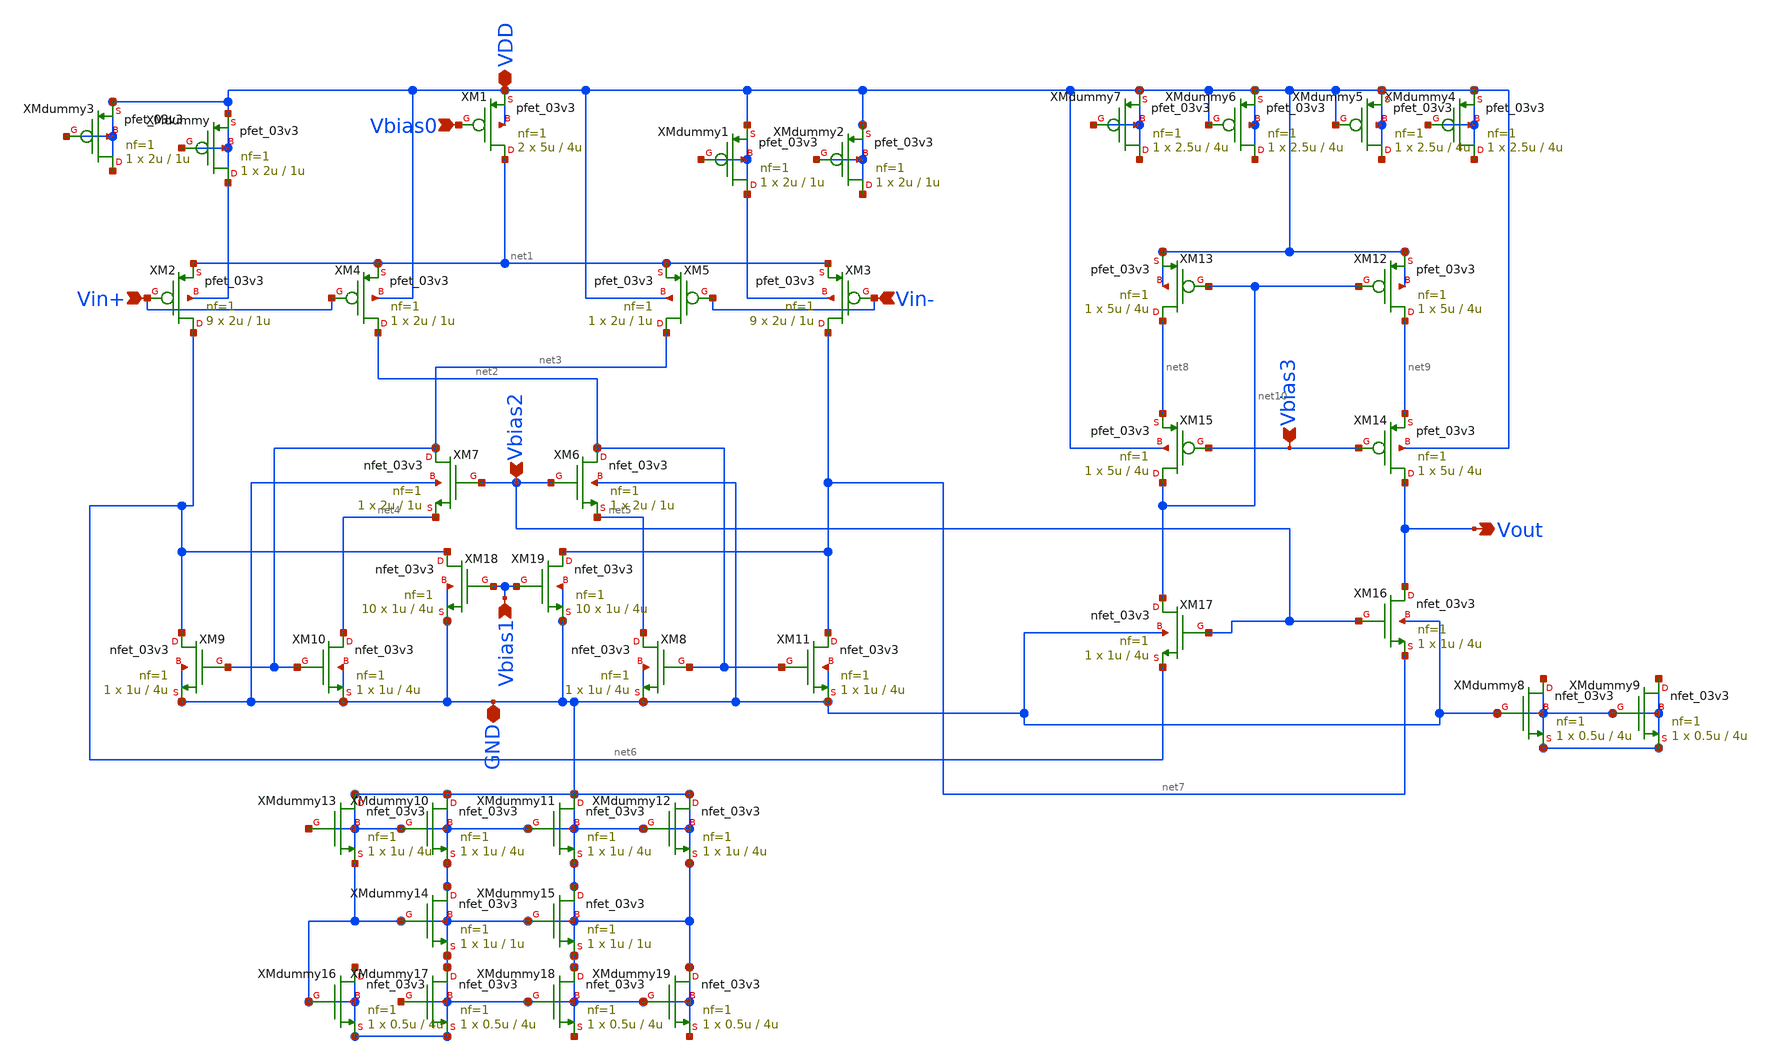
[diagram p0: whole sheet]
** sch_path: analog/B04_OTA.sch
**.subckt B04_OTA VDD Vbias0 Vin+ Vin- Vout Vbias3 Vbias2 GND Vbias1
*.iopin VDD
*.ipin Vbias0
*.ipin Vin+
*.ipin Vin-
*.opin Vout
*.ipin Vbias3
*.ipin Vbias2
*.iopin GND
*.ipin Vbias1
XM1 net1 Vbias0 VDD VDD pfet_03v3 L=4u W=5u nf=1 ad='int((nf+1)/2) * W/nf * 0.18u' as='int((nf+2)/2) * W/nf * 0.18u'
+ pd='2*int((nf+1)/2) * (W/nf + 0.18u)' ps='2*int((nf+2)/2) * (W/nf + 0.18u)' nrd='0.18u / W' nrs='0.18u / W'
+ sa=0 sb=0 sd=0 m=2
XM2 net6 Vin+ net1 VDD pfet_03v3 L=1u W=2u nf=1 ad='int((nf+1)/2) * W/nf * 0.18u' as='int((nf+2)/2) * W/nf * 0.18u'
+ pd='2*int((nf+1)/2) * (W/nf + 0.18u)' ps='2*int((nf+2)/2) * (W/nf + 0.18u)' nrd='0.18u / W' nrs='0.18u / W'
+ sa=0 sb=0 sd=0 m=9
XM3 net7 Vin- net1 VDD pfet_03v3 L=1u W=2u nf=1 ad='int((nf+1)/2) * W/nf * 0.18u' as='int((nf+2)/2) * W/nf * 0.18u'
+ pd='2*int((nf+1)/2) * (W/nf + 0.18u)' ps='2*int((nf+2)/2) * (W/nf + 0.18u)' nrd='0.18u / W' nrs='0.18u / W'
+ sa=0 sb=0 sd=0 m=9
XM4 net2 Vin+ net1 VDD pfet_03v3 L=1u W=2u nf=1 ad='int((nf+1)/2) * W/nf * 0.18u' as='int((nf+2)/2) * W/nf * 0.18u'
+ pd='2*int((nf+1)/2) * (W/nf + 0.18u)' ps='2*int((nf+2)/2) * (W/nf + 0.18u)' nrd='0.18u / W' nrs='0.18u / W'
+ sa=0 sb=0 sd=0 m=1
XM5 net3 Vin- net1 VDD pfet_03v3 L=1u W=2u nf=1 ad='int((nf+1)/2) * W/nf * 0.18u' as='int((nf+2)/2) * W/nf * 0.18u'
+ pd='2*int((nf+1)/2) * (W/nf + 0.18u)' ps='2*int((nf+2)/2) * (W/nf + 0.18u)' nrd='0.18u / W' nrs='0.18u / W'
+ sa=0 sb=0 sd=0 m=1
XM6 net2 Vbias2 net5 GND nfet_03v3 L=1u W=2u nf=1 ad='int((nf+1)/2) * W/nf * 0.18u' as='int((nf+2)/2) * W/nf * 0.18u'
+ pd='2*int((nf+1)/2) * (W/nf + 0.18u)' ps='2*int((nf+2)/2) * (W/nf + 0.18u)' nrd='0.18u / W' nrs='0.18u / W'
+ sa=0 sb=0 sd=0 m=1
XM7 net3 Vbias2 net4 GND nfet_03v3 L=1u W=2u nf=1 ad='int((nf+1)/2) * W/nf * 0.18u' as='int((nf+2)/2) * W/nf * 0.18u'
+ pd='2*int((nf+1)/2) * (W/nf + 0.18u)' ps='2*int((nf+2)/2) * (W/nf + 0.18u)' nrd='0.18u / W' nrs='0.18u / W'
+ sa=0 sb=0 sd=0 m=1
XM8 net5 net2 GND GND nfet_03v3 L=4u W=1u nf=1 ad='int((nf+1)/2) * W/nf * 0.18u' as='int((nf+2)/2) * W/nf * 0.18u'
+ pd='2*int((nf+1)/2) * (W/nf + 0.18u)' ps='2*int((nf+2)/2) * (W/nf + 0.18u)' nrd='0.18u / W' nrs='0.18u / W'
+ sa=0 sb=0 sd=0 m=1
XM9 net6 net3 GND GND nfet_03v3 L=4u W=1u nf=1 ad='int((nf+1)/2) * W/nf * 0.18u' as='int((nf+2)/2) * W/nf * 0.18u'
+ pd='2*int((nf+1)/2) * (W/nf + 0.18u)' ps='2*int((nf+2)/2) * (W/nf + 0.18u)' nrd='0.18u / W' nrs='0.18u / W'
+ sa=0 sb=0 sd=0 m=1
XM10 net4 net3 GND GND nfet_03v3 L=4u W=1u nf=1 ad='int((nf+1)/2) * W/nf * 0.18u' as='int((nf+2)/2) * W/nf * 0.18u'
+ pd='2*int((nf+1)/2) * (W/nf + 0.18u)' ps='2*int((nf+2)/2) * (W/nf + 0.18u)' nrd='0.18u / W' nrs='0.18u / W'
+ sa=0 sb=0 sd=0 m=1
XM11 net7 net2 GND GND nfet_03v3 L=4u W=1u nf=1 ad='int((nf+1)/2) * W/nf * 0.18u' as='int((nf+2)/2) * W/nf * 0.18u'
+ pd='2*int((nf+1)/2) * (W/nf + 0.18u)' ps='2*int((nf+2)/2) * (W/nf + 0.18u)' nrd='0.18u / W' nrs='0.18u / W'
+ sa=0 sb=0 sd=0 m=1
XM12 net9 net10 VDD VDD pfet_03v3 L=4u W=5u nf=1 ad='int((nf+1)/2) * W/nf * 0.18u' as='int((nf+2)/2) * W/nf * 0.18u'
+ pd='2*int((nf+1)/2) * (W/nf + 0.18u)' ps='2*int((nf+2)/2) * (W/nf + 0.18u)' nrd='0.18u / W' nrs='0.18u / W'
+ sa=0 sb=0 sd=0 m=1
XM13 net8 net10 VDD VDD pfet_03v3 L=4u W=5u nf=1 ad='int((nf+1)/2) * W/nf * 0.18u' as='int((nf+2)/2) * W/nf * 0.18u'
+ pd='2*int((nf+1)/2) * (W/nf + 0.18u)' ps='2*int((nf+2)/2) * (W/nf + 0.18u)' nrd='0.18u / W' nrs='0.18u / W'
+ sa=0 sb=0 sd=0 m=1
XM14 Vout Vbias3 net9 VDD pfet_03v3 L=4u W=5u nf=1 ad='int((nf+1)/2) * W/nf * 0.18u' as='int((nf+2)/2) * W/nf * 0.18u'
+ pd='2*int((nf+1)/2) * (W/nf + 0.18u)' ps='2*int((nf+2)/2) * (W/nf + 0.18u)' nrd='0.18u / W' nrs='0.18u / W'
+ sa=0 sb=0 sd=0 m=1
XM15 net10 Vbias3 net8 VDD pfet_03v3 L=4u W=5u nf=1 ad='int((nf+1)/2) * W/nf * 0.18u' as='int((nf+2)/2) * W/nf * 0.18u'
+ pd='2*int((nf+1)/2) * (W/nf + 0.18u)' ps='2*int((nf+2)/2) * (W/nf + 0.18u)' nrd='0.18u / W' nrs='0.18u / W'
+ sa=0 sb=0 sd=0 m=1
XM16 Vout Vbias2 net7 GND nfet_03v3 L=4u W=1u nf=1 ad='int((nf+1)/2) * W/nf * 0.18u' as='int((nf+2)/2) * W/nf * 0.18u'
+ pd='2*int((nf+1)/2) * (W/nf + 0.18u)' ps='2*int((nf+2)/2) * (W/nf + 0.18u)' nrd='0.18u / W' nrs='0.18u / W'
+ sa=0 sb=0 sd=0 m=1
XM17 net10 Vbias2 net6 GND nfet_03v3 L=4u W=1u nf=1 ad='int((nf+1)/2) * W/nf * 0.18u' as='int((nf+2)/2) * W/nf * 0.18u'
+ pd='2*int((nf+1)/2) * (W/nf + 0.18u)' ps='2*int((nf+2)/2) * (W/nf + 0.18u)' nrd='0.18u / W' nrs='0.18u / W'
+ sa=0 sb=0 sd=0 m=1
XM18 net6 Vbias1 GND GND nfet_03v3 L=4u W=1u nf=1 ad='int((nf+1)/2) * W/nf * 0.18u' as='int((nf+2)/2) * W/nf * 0.18u'
+ pd='2*int((nf+1)/2) * (W/nf + 0.18u)' ps='2*int((nf+2)/2) * (W/nf + 0.18u)' nrd='0.18u / W' nrs='0.18u / W'
+ sa=0 sb=0 sd=0 m=10
XM19 net7 Vbias1 GND GND nfet_03v3 L=4u W=1u nf=1 ad='int((nf+1)/2) * W/nf * 0.18u' as='int((nf+2)/2) * W/nf * 0.18u'
+ pd='2*int((nf+1)/2) * (W/nf + 0.18u)' ps='2*int((nf+2)/2) * (W/nf + 0.18u)' nrd='0.18u / W' nrs='0.18u / W'
+ sa=0 sb=0 sd=0 m=10
XMdummy VDD VDD VDD VDD pfet_03v3 L=1u W=2u nf=1 ad='int((nf+1)/2) * W/nf * 0.18u' as='int((nf+2)/2) * W/nf * 0.18u'
+ pd='2*int((nf+1)/2) * (W/nf + 0.18u)' ps='2*int((nf+2)/2) * (W/nf + 0.18u)' nrd='0.18u / W' nrs='0.18u / W'
+ sa=0 sb=0 sd=0 m=1
XMdummy1 VDD VDD VDD VDD pfet_03v3 L=1u W=2u nf=1 ad='int((nf+1)/2) * W/nf * 0.18u' as='int((nf+2)/2) * W/nf * 0.18u'
+ pd='2*int((nf+1)/2) * (W/nf + 0.18u)' ps='2*int((nf+2)/2) * (W/nf + 0.18u)' nrd='0.18u / W' nrs='0.18u / W'
+ sa=0 sb=0 sd=0 m=1
XMdummy2 VDD VDD VDD VDD pfet_03v3 L=1u W=2u nf=1 ad='int((nf+1)/2) * W/nf * 0.18u' as='int((nf+2)/2) * W/nf * 0.18u'
+ pd='2*int((nf+1)/2) * (W/nf + 0.18u)' ps='2*int((nf+2)/2) * (W/nf + 0.18u)' nrd='0.18u / W' nrs='0.18u / W'
+ sa=0 sb=0 sd=0 m=1
XMdummy3 VDD VDD VDD VDD pfet_03v3 L=1u W=2u nf=1 ad='int((nf+1)/2) * W/nf * 0.18u' as='int((nf+2)/2) * W/nf * 0.18u'
+ pd='2*int((nf+1)/2) * (W/nf + 0.18u)' ps='2*int((nf+2)/2) * (W/nf + 0.18u)' nrd='0.18u / W' nrs='0.18u / W'
+ sa=0 sb=0 sd=0 m=1
XMdummy4 VDD VDD VDD VDD pfet_03v3 L=4u W=2.5u nf=1 ad='int((nf+1)/2) * W/nf * 0.18u' as='int((nf+2)/2) * W/nf * 0.18u'
+ pd='2*int((nf+1)/2) * (W/nf + 0.18u)' ps='2*int((nf+2)/2) * (W/nf + 0.18u)' nrd='0.18u / W' nrs='0.18u / W'
+ sa=0 sb=0 sd=0 m=1
XMdummy5 VDD VDD VDD VDD pfet_03v3 L=4u W=2.5u nf=1 ad='int((nf+1)/2) * W/nf * 0.18u' as='int((nf+2)/2) * W/nf * 0.18u'
+ pd='2*int((nf+1)/2) * (W/nf + 0.18u)' ps='2*int((nf+2)/2) * (W/nf + 0.18u)' nrd='0.18u / W' nrs='0.18u / W'
+ sa=0 sb=0 sd=0 m=1
XMdummy6 VDD VDD VDD VDD pfet_03v3 L=4u W=2.5u nf=1 ad='int((nf+1)/2) * W/nf * 0.18u' as='int((nf+2)/2) * W/nf * 0.18u'
+ pd='2*int((nf+1)/2) * (W/nf + 0.18u)' ps='2*int((nf+2)/2) * (W/nf + 0.18u)' nrd='0.18u / W' nrs='0.18u / W'
+ sa=0 sb=0 sd=0 m=1
XMdummy7 VDD VDD VDD VDD pfet_03v3 L=4u W=2.5u nf=1 ad='int((nf+1)/2) * W/nf * 0.18u' as='int((nf+2)/2) * W/nf * 0.18u'
+ pd='2*int((nf+1)/2) * (W/nf + 0.18u)' ps='2*int((nf+2)/2) * (W/nf + 0.18u)' nrd='0.18u / W' nrs='0.18u / W'
+ sa=0 sb=0 sd=0 m=1
XMdummy8 GND GND GND GND nfet_03v3 L=4u W=0.5u nf=1 ad='int((nf+1)/2) * W/nf * 0.18u' as='int((nf+2)/2) * W/nf * 0.18u'
+ pd='2*int((nf+1)/2) * (W/nf + 0.18u)' ps='2*int((nf+2)/2) * (W/nf + 0.18u)' nrd='0.18u / W' nrs='0.18u / W'
+ sa=0 sb=0 sd=0 m=1
XMdummy9 GND GND GND GND nfet_03v3 L=4u W=0.5u nf=1 ad='int((nf+1)/2) * W/nf * 0.18u' as='int((nf+2)/2) * W/nf * 0.18u'
+ pd='2*int((nf+1)/2) * (W/nf + 0.18u)' ps='2*int((nf+2)/2) * (W/nf + 0.18u)' nrd='0.18u / W' nrs='0.18u / W'
+ sa=0 sb=0 sd=0 m=1
XMdummy10 GND GND GND GND nfet_03v3 L=4u W=1u nf=1 ad='int((nf+1)/2) * W/nf * 0.18u' as='int((nf+2)/2) * W/nf * 0.18u'
+ pd='2*int((nf+1)/2) * (W/nf + 0.18u)' ps='2*int((nf+2)/2) * (W/nf + 0.18u)' nrd='0.18u / W' nrs='0.18u / W'
+ sa=0 sb=0 sd=0 m=1
XMdummy11 GND GND GND GND nfet_03v3 L=4u W=1u nf=1 ad='int((nf+1)/2) * W/nf * 0.18u' as='int((nf+2)/2) * W/nf * 0.18u'
+ pd='2*int((nf+1)/2) * (W/nf + 0.18u)' ps='2*int((nf+2)/2) * (W/nf + 0.18u)' nrd='0.18u / W' nrs='0.18u / W'
+ sa=0 sb=0 sd=0 m=1
XMdummy12 GND GND GND GND nfet_03v3 L=4u W=1u nf=1 ad='int((nf+1)/2) * W/nf * 0.18u' as='int((nf+2)/2) * W/nf * 0.18u'
+ pd='2*int((nf+1)/2) * (W/nf + 0.18u)' ps='2*int((nf+2)/2) * (W/nf + 0.18u)' nrd='0.18u / W' nrs='0.18u / W'
+ sa=0 sb=0 sd=0 m=1
XMdummy13 GND GND GND GND nfet_03v3 L=4u W=1u nf=1 ad='int((nf+1)/2) * W/nf * 0.18u' as='int((nf+2)/2) * W/nf * 0.18u'
+ pd='2*int((nf+1)/2) * (W/nf + 0.18u)' ps='2*int((nf+2)/2) * (W/nf + 0.18u)' nrd='0.18u / W' nrs='0.18u / W'
+ sa=0 sb=0 sd=0 m=1
XMdummy14 GND GND GND GND nfet_03v3 L=1u W=1u nf=1 ad='int((nf+1)/2) * W/nf * 0.18u' as='int((nf+2)/2) * W/nf * 0.18u'
+ pd='2*int((nf+1)/2) * (W/nf + 0.18u)' ps='2*int((nf+2)/2) * (W/nf + 0.18u)' nrd='0.18u / W' nrs='0.18u / W'
+ sa=0 sb=0 sd=0 m=1
XMdummy15 GND GND GND GND nfet_03v3 L=1u W=1u nf=1 ad='int((nf+1)/2) * W/nf * 0.18u' as='int((nf+2)/2) * W/nf * 0.18u'
+ pd='2*int((nf+1)/2) * (W/nf + 0.18u)' ps='2*int((nf+2)/2) * (W/nf + 0.18u)' nrd='0.18u / W' nrs='0.18u / W'
+ sa=0 sb=0 sd=0 m=1
XMdummy16 GND GND GND GND nfet_03v3 L=4u W=0.5u nf=1 ad='int((nf+1)/2) * W/nf * 0.18u' as='int((nf+2)/2) * W/nf * 0.18u'
+ pd='2*int((nf+1)/2) * (W/nf + 0.18u)' ps='2*int((nf+2)/2) * (W/nf + 0.18u)' nrd='0.18u / W' nrs='0.18u / W'
+ sa=0 sb=0 sd=0 m=1
XMdummy17 GND GND GND GND nfet_03v3 L=4u W=0.5u nf=1 ad='int((nf+1)/2) * W/nf * 0.18u' as='int((nf+2)/2) * W/nf * 0.18u'
+ pd='2*int((nf+1)/2) * (W/nf + 0.18u)' ps='2*int((nf+2)/2) * (W/nf + 0.18u)' nrd='0.18u / W' nrs='0.18u / W'
+ sa=0 sb=0 sd=0 m=1
XMdummy18 GND GND GND GND nfet_03v3 L=4u W=0.5u nf=1 ad='int((nf+1)/2) * W/nf * 0.18u' as='int((nf+2)/2) * W/nf * 0.18u'
+ pd='2*int((nf+1)/2) * (W/nf + 0.18u)' ps='2*int((nf+2)/2) * (W/nf + 0.18u)' nrd='0.18u / W' nrs='0.18u / W'
+ sa=0 sb=0 sd=0 m=1
XMdummy19 GND GND GND GND nfet_03v3 L=4u W=0.5u nf=1 ad='int((nf+1)/2) * W/nf * 0.18u' as='int((nf+2)/2) * W/nf * 0.18u'
+ pd='2*int((nf+1)/2) * (W/nf + 0.18u)' ps='2*int((nf+2)/2) * (W/nf + 0.18u)' nrd='0.18u / W' nrs='0.18u / W'
+ sa=0 sb=0 sd=0 m=1
**.ends
.end
